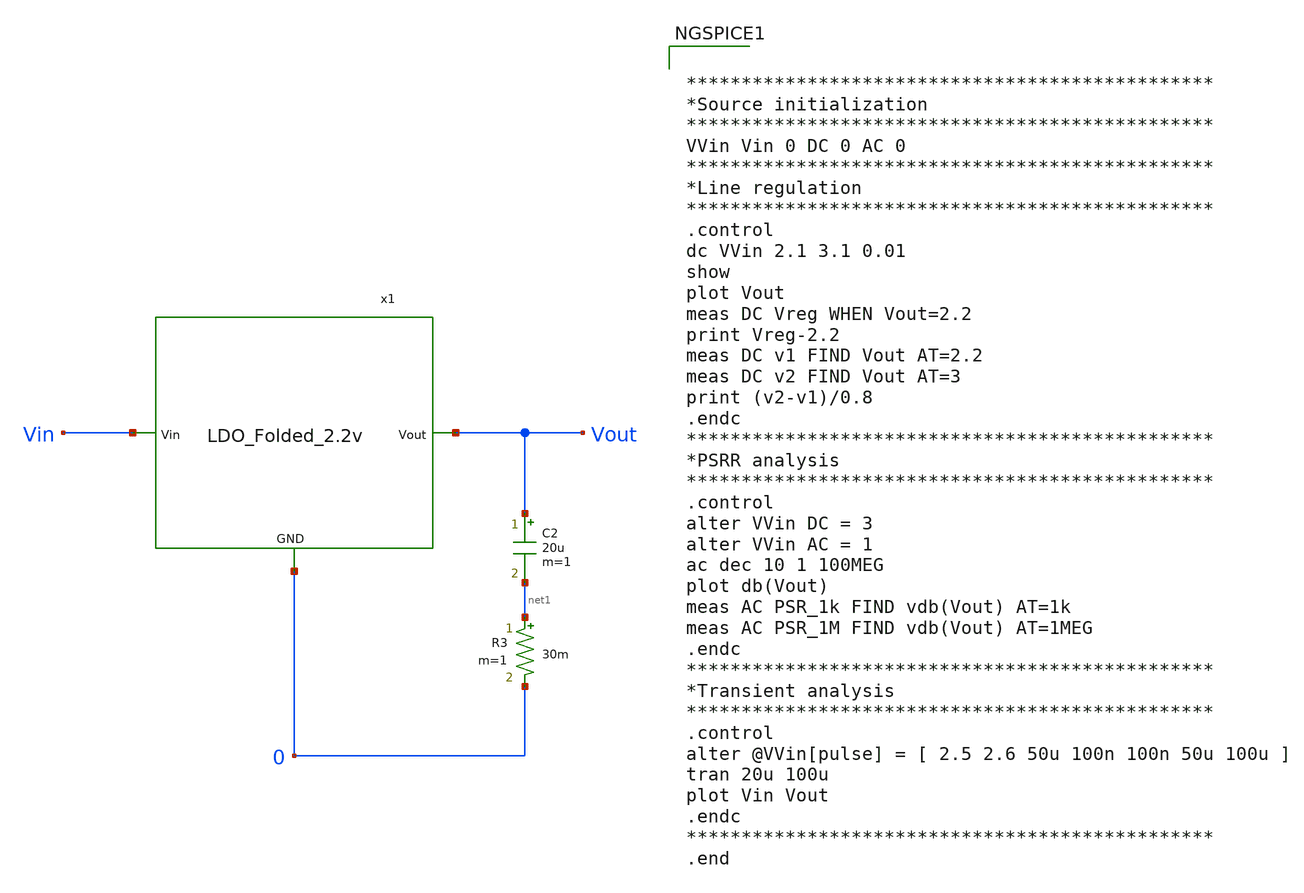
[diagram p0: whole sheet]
** sch_path: Analog_Blocks/LDO/Testbench/LDO_Folded_2.2v_meas.sch
**.subckt LDO_Folded_2.2v_meas
C2 Vout net1 20u m=1
R3 net1 0 30m m=1
x1 Vin Vout 0 LDO_Folded_2.2v
**** begin user architecture code


************************************************
*Source initialization
************************************************
VVin Vin 0 DC 0 AC 0
************************************************
*Line regulation
************************************************
.control
dc VVin 2.1 3.1 0.01
show
plot Vout
meas DC Vreg WHEN Vout=2.2
print Vreg-2.2
meas DC v1 FIND Vout AT=2.2
meas DC v2 FIND Vout AT=3
print (v2-v1)/0.8
.endc
************************************************
*PSRR analysis
************************************************
.control
alter VVin DC = 3
alter VVin AC = 1
ac dec 10 1 100MEG
plot db(Vout)
meas AC PSR_1k FIND vdb(Vout) AT=1k
meas AC PSR_1M FIND vdb(Vout) AT=1MEG
.endc
************************************************
*Transient analysis
************************************************
.control
alter @VVin[pulse] = [ 2.5 2.6 50u 100n 100n 50u 100u ]
tran 20u 100u
plot Vin Vout
.endc
************************************************
.end



.include ~/Analog_blocks/models/skywater-pdk/libraries/sky130_fd_pr/latest/cells/nfet_01v8/sky130_fd_pr__nfet_01v8__tt.corner.spice
.include ~/Analog_blocks/models/skywater-pdk/libraries/sky130_fd_pr/latest/cells/nfet_01v8_lvt/sky130_fd_pr__nfet_01v8_lvt__tt.corner.spice
.include ~/Analog_blocks/models/skywater-pdk/libraries/sky130_fd_pr/latest/cells/pfet_01v8/sky130_fd_pr__pfet_01v8__tt.corner.spice
.include ~/Analog_blocks/models/skywater-pdk/libraries/sky130_fd_pr/latest/cells/nfet_03v3_nvt/sky130_fd_pr__nfet_03v3_nvt__tt.corner.spice
.include ~/Analog_blocks/models/skywater-pdk/libraries/sky130_fd_pr/latest/cells/nfet_05v0_nvt/sky130_fd_pr__nfet_05v0_nvt__tt.corner.spice
.include ~/Analog_blocks/models/skywater-pdk/libraries/sky130_fd_pr/latest/cells/esd_nfet_01v8/sky130_fd_pr__esd_nfet_01v8__tt.corner.spice
.include ~/Analog_blocks/models/skywater-pdk/libraries/sky130_fd_pr/latest/cells/pfet_01v8_lvt/sky130_fd_pr__pfet_01v8_lvt__tt.corner.spice
.include ~/Analog_blocks/models/skywater-pdk/libraries/sky130_fd_pr/latest/cells/pfet_01v8_hvt/sky130_fd_pr__pfet_01v8_hvt__tt.corner.spice
.include ~/Analog_blocks/models/skywater-pdk/libraries/sky130_fd_pr/latest/cells/esd_pfet_g5v0d10v5/sky130_fd_pr__esd_pfet_g5v0d10v5__tt.corner.spice
.include ~/Analog_blocks/models/skywater-pdk/libraries/sky130_fd_pr/latest/cells/pfet_g5v0d10v5/sky130_fd_pr__pfet_g5v0d10v5__tt.corner.spice
.include ~/Analog_blocks/models/skywater-pdk/libraries/sky130_fd_pr/latest/cells/pfet_g5v0d16v0/sky130_fd_pr__pfet_g5v0d16v0__tt.corner.spice
.include ~/Analog_blocks/models/skywater-pdk/libraries/sky130_fd_pr/latest/cells/nfet_g5v0d10v5/sky130_fd_pr__nfet_g5v0d10v5__tt.corner.spice
.include ~/Analog_blocks/models/skywater-pdk/libraries/sky130_fd_pr/latest/cells/nfet_g5v0d16v0/sky130_fd_pr__nfet_g5v0d16v0__tt_discrete.corner.spice
.include ~/Analog_blocks/models/skywater-pdk/libraries/sky130_fd_pr/latest/cells/esd_nfet_g5v0d10v5/sky130_fd_pr__esd_nfet_g5v0d10v5__tt.corner.spice
.include ~/Analog_blocks/models/skywater-pdk/libraries/sky130_fd_pr/latest/models/corners/tt/nonfet.spice
* Mismatch parameters
.include ~/Analog_blocks/models/skywater-pdk/libraries/sky130_fd_pr/latest/cells/nfet_01v8/sky130_fd_pr__nfet_01v8__mismatch.corner.spice
.include ~/Analog_blocks/models/skywater-pdk/libraries/sky130_fd_pr/latest/cells/pfet_01v8/sky130_fd_pr__pfet_01v8__mismatch.corner.spice
.include ~/Analog_blocks/models/skywater-pdk/libraries/sky130_fd_pr/latest/cells/nfet_01v8_lvt/sky130_fd_pr__nfet_01v8_lvt__mismatch.corner.spice
.include ~/Analog_blocks/models/skywater-pdk/libraries/sky130_fd_pr/latest/cells/pfet_01v8_lvt/sky130_fd_pr__pfet_01v8_lvt__mismatch.corner.spice
.include ~/Analog_blocks/models/skywater-pdk/libraries/sky130_fd_pr/latest/cells/pfet_01v8_hvt/sky130_fd_pr__pfet_01v8_hvt__mismatch.corner.spice
.include ~/Analog_blocks/models/skywater-pdk/libraries/sky130_fd_pr/latest/cells/nfet_g5v0d10v5/sky130_fd_pr__nfet_g5v0d10v5__mismatch.corner.spice
.include ~/Analog_blocks/models/skywater-pdk/libraries/sky130_fd_pr/latest/cells/pfet_g5v0d10v5/sky130_fd_pr__pfet_g5v0d10v5__mismatch.corner.spice
.include ~/Analog_blocks/models/skywater-pdk/libraries/sky130_fd_pr/latest/cells/nfet_05v0_nvt/sky130_fd_pr__nfet_05v0_nvt__mismatch.corner.spice
.include ~/Analog_blocks/models/skywater-pdk/libraries/sky130_fd_pr/latest/cells/nfet_03v3_nvt/sky130_fd_pr__nfet_03v3_nvt__mismatch.corner.spice
* Resistor
.include ~/Analog_blocks/models/skywater-pdk/libraries/sky130_fd_pr/latest/models/r+c/res_typical__cap_typical.spice
.include ~/Analog_blocks/models/skywater-pdk/libraries/sky130_fd_pr/latest/models/r+c/res_typical__cap_typical__lin.spice
* Special cells
.include ~/Analog_blocks/models/skywater-pdk/libraries/sky130_fd_pr/latest/models/corners/tt/specialized_cells.spice
* All models
.include ~/Analog_blocks/models/skywater-pdk/libraries/sky130_fd_pr/latest/models/all.spice
* Corner
.include ~/Analog_blocks/models/skywater-pdk/libraries/sky130_fd_pr/latest/models/corners/tt/rf.spice

**** end user architecture code
**.ends

* expanding   symbol:
*+  /home/eslam/Analog_blocks/Analog_Blocks/LDO/Schematic/LDO_Folded_2.2v/LDO_Folded_2.2v.sym # of pins=3
** sym_path: Analog_blocks/Analog_Blocks/LDO/Schematic/LDO_Folded_2.2v/LDO_Folded_2.2v.sym
** sch_path: Analog_blocks/Analog_Blocks/LDO/Schematic/LDO_Folded_2.2v/LDO_Folded_2.2v.sch
.subckt LDO_Folded_2.2v Vin Vout GND
*.ipin Vin
*.ipin GND
*.opin Vout
XR1 net1 Vout GND sky130_fd_pr__res_xhigh_po W=1 L=60 mult=1 m=1
XR2 GND net1 GND sky130_fd_pr__res_xhigh_po W=1 L=50 mult=1 m=1
XC1 Vout net1 sky130_fd_pr__cap_mim_m3_2 W=1 L=1 MF=1 m=1
XM1 Vout net2 Vin Vin sky130_fd_pr__pfet_g5v0d10v5 L=0.5 W=20 nf=1 ad='int((nf+1)/2) * W/nf * 0.29' as='int((nf+2)/2) * W/nf * 0.29'
+ pd='2*int((nf+1)/2) * (W/nf + 0.29)' ps='2*int((nf+2)/2) * (W/nf + 0.29)' nrd='0.29 / W' nrs='0.29 / W'
+ sa=0 sb=0 sd=0 mult=1000 m=1000
x1 Vin net2 net1 net3 net3 GND Error_amplifier_Folded
x2 net3 Vin GND Bandgap5v
.ends


* expanding   symbol:
*+  /home/eslam/Analog_blocks/Analog_Blocks/LDO/Schematic/LDO_Folded_2.2v/Error_amplifier_Folded.sym # of pins=6
** sym_path: Analog_Blocks/LDO/Schematic/LDO_Folded_1.8v/Error_amplifier_Folded.sym
** sch_path: Analog_Blocks/LDO/Schematic/LDO_Folded_1.8v/Error_amplifier_Folded.sch
.subckt Error_amplifier_Folded VDD Vout Vp Vn Ibias GND
*.ipin VDD
*.ipin GND
*.ipin Vp
*.ipin Vn
*.opin Vout
*.ipin Ibias
XM1 net3 Vp net1 GND sky130_fd_pr__nfet_g5v0d10v5 L=0.5 W=50 nf=1 ad='int((nf+1)/2) * W/nf * 0.29' as='int((nf+2)/2) * W/nf * 0.29'
+ pd='2*int((nf+1)/2) * (W/nf + 0.29)' ps='2*int((nf+2)/2) * (W/nf + 0.29)' nrd='0.29 / W' nrs='0.29 / W'
+ sa=0 sb=0 sd=0 mult=1 m=1
XM2 net2 Vn net1 GND sky130_fd_pr__nfet_g5v0d10v5 L=0.5 W=50 nf=1 ad='int((nf+1)/2) * W/nf * 0.29' as='int((nf+2)/2) * W/nf * 0.29'
+ pd='2*int((nf+1)/2) * (W/nf + 0.29)' ps='2*int((nf+2)/2) * (W/nf + 0.29)' nrd='0.29 / W' nrs='0.29 / W'
+ sa=0 sb=0 sd=0 mult=1 m=1
XM9 Vout net4 GND GND sky130_fd_pr__nfet_g5v0d10v5 L=2 W=6 nf=1 ad='int((nf+1)/2) * W/nf * 0.29' as='int((nf+2)/2) * W/nf * 0.29'
+ pd='2*int((nf+1)/2) * (W/nf + 0.29)' ps='2*int((nf+2)/2) * (W/nf + 0.29)' nrd='0.29 / W' nrs='0.29 / W'
+ sa=0 sb=0 sd=0 mult=1 m=1
XM6 net4 net6 net3 VDD sky130_fd_pr__pfet_g5v0d10v5 L=0.5 W=40 nf=1 ad='int((nf+1)/2) * W/nf * 0.29'
+ as='int((nf+2)/2) * W/nf * 0.29' pd='2*int((nf+1)/2) * (W/nf + 0.29)' ps='2*int((nf+2)/2) * (W/nf + 0.29)'
+ nrd='0.29 / W' nrs='0.29 / W' sa=0 sb=0 sd=0 mult=1 m=1
XM5 net2 net5 VDD VDD sky130_fd_pr__pfet_g5v0d10v5 L=0.5 W=40 nf=1 ad='int((nf+1)/2) * W/nf * 0.29' as='int((nf+2)/2) * W/nf * 0.29'
+ pd='2*int((nf+1)/2) * (W/nf + 0.29)' ps='2*int((nf+2)/2) * (W/nf + 0.29)' nrd='0.29 / W' nrs='0.29 / W'
+ sa=0 sb=0 sd=0 mult=1 m=1
XM4 net3 net5 VDD VDD sky130_fd_pr__pfet_g5v0d10v5 L=0.5 W=40 nf=1 ad='int((nf+1)/2) * W/nf * 0.29' as='int((nf+2)/2) * W/nf * 0.29'
+ pd='2*int((nf+1)/2) * (W/nf + 0.29)' ps='2*int((nf+2)/2) * (W/nf + 0.29)' nrd='0.29 / W' nrs='0.29 / W'
+ sa=0 sb=0 sd=0 mult=1 m=1
XM3 net1 Ibias GND GND sky130_fd_pr__nfet_g5v0d10v5 L=0.9 W=12 nf=1 ad='int((nf+1)/2) * W/nf * 0.29'
+ as='int((nf+2)/2) * W/nf * 0.29' pd='2*int((nf+1)/2) * (W/nf + 0.29)' ps='2*int((nf+2)/2) * (W/nf + 0.29)'
+ nrd='0.29 / W' nrs='0.29 / W' sa=0 sb=0 sd=0 mult=1 m=1
XM7 Vout net6 net2 VDD sky130_fd_pr__pfet_g5v0d10v5 L=0.5 W=40 nf=1 ad='int((nf+1)/2) * W/nf * 0.29'
+ as='int((nf+2)/2) * W/nf * 0.29' pd='2*int((nf+1)/2) * (W/nf + 0.29)' ps='2*int((nf+2)/2) * (W/nf + 0.29)'
+ nrd='0.29 / W' nrs='0.29 / W' sa=0 sb=0 sd=0 mult=1 m=1
XM8 net4 net4 GND GND sky130_fd_pr__nfet_g5v0d10v5 L=2 W=6 nf=1 ad='int((nf+1)/2) * W/nf * 0.29' as='int((nf+2)/2) * W/nf * 0.29'
+ pd='2*int((nf+1)/2) * (W/nf + 0.29)' ps='2*int((nf+2)/2) * (W/nf + 0.29)' nrd='0.29 / W' nrs='0.29 / W'
+ sa=0 sb=0 sd=0 mult=1 m=1
XM10 Ibias Ibias GND GND sky130_fd_pr__nfet_g5v0d10v5 L=0.9 W=12 nf=1 ad='int((nf+1)/2) * W/nf * 0.29'
+ as='int((nf+2)/2) * W/nf * 0.29' pd='2*int((nf+1)/2) * (W/nf + 0.29)' ps='2*int((nf+2)/2) * (W/nf + 0.29)'
+ nrd='0.29 / W' nrs='0.29 / W' sa=0 sb=0 sd=0 mult=1 m=1
XM11 net5 Ibias GND GND sky130_fd_pr__nfet_g5v0d10v5 L=0.9 W=6 nf=1 ad='int((nf+1)/2) * W/nf * 0.29'
+ as='int((nf+2)/2) * W/nf * 0.29' pd='2*int((nf+1)/2) * (W/nf + 0.29)' ps='2*int((nf+2)/2) * (W/nf + 0.29)'
+ nrd='0.29 / W' nrs='0.29 / W' sa=0 sb=0 sd=0 mult=1 m=1
XM12 net6 Ibias GND GND sky130_fd_pr__nfet_g5v0d10v5 L=0.9 W=6 nf=1 ad='int((nf+1)/2) * W/nf * 0.29'
+ as='int((nf+2)/2) * W/nf * 0.29' pd='2*int((nf+1)/2) * (W/nf + 0.29)' ps='2*int((nf+2)/2) * (W/nf + 0.29)'
+ nrd='0.29 / W' nrs='0.29 / W' sa=0 sb=0 sd=0 mult=1 m=1
XM13 net5 net5 VDD VDD sky130_fd_pr__pfet_g5v0d10v5 L=0.5 W=13.5 nf=1 ad='int((nf+1)/2) * W/nf * 0.29'
+ as='int((nf+2)/2) * W/nf * 0.29' pd='2*int((nf+1)/2) * (W/nf + 0.29)' ps='2*int((nf+2)/2) * (W/nf + 0.29)'
+ nrd='0.29 / W' nrs='0.29 / W' sa=0 sb=0 sd=0 mult=1 m=1
XM14 net6 net6 VDD VDD sky130_fd_pr__pfet_g5v0d10v5 L=1 W=2 nf=1 ad='int((nf+1)/2) * W/nf * 0.29' as='int((nf+2)/2) * W/nf * 0.29'
+ pd='2*int((nf+1)/2) * (W/nf + 0.29)' ps='2*int((nf+2)/2) * (W/nf + 0.29)' nrd='0.29 / W' nrs='0.29 / W'
+ sa=0 sb=0 sd=0 mult=1 m=1
.ends


* expanding   symbol:
*+  /home/eslam/Analog_blocks/Analog_Blocks/LDO/Schematic/LDO_Folded_2.2v/Bandgap5v.sym # of pins=3
** sym_path: Analog_Blocks/Bandgap/Schematics/BGR5v/Bandgap5v.sym
** sch_path: Analog_Blocks/Bandgap/Schematics/BGR5v/Bandgap5v.sch
.subckt Bandgap5v Vref VDD GND
*.ipin VDD
*.ipin GND
*.opin Vref
XQ1 GND GND net3 sky130_fd_pr__pnp_05v5_W0p68L0p68 m=1
XQ2 GND GND net1 sky130_fd_pr__pnp_05v5_W0p68L0p68 m=1
XQ3 GND GND net1 sky130_fd_pr__pnp_05v5_W0p68L0p68 m=1
XQ4 GND GND net1 sky130_fd_pr__pnp_05v5_W0p68L0p68 m=1
XQ5 GND GND net1 sky130_fd_pr__pnp_05v5_W0p68L0p68 m=1
XQ6 GND GND net1 sky130_fd_pr__pnp_05v5_W0p68L0p68 m=1
XQ7 GND GND net1 sky130_fd_pr__pnp_05v5_W0p68L0p68 m=1
XQ8 GND GND net1 sky130_fd_pr__pnp_05v5_W0p68L0p68 m=1
XQ9 GND GND net1 sky130_fd_pr__pnp_05v5_W0p68L0p68 m=1
XM2 net4 net5 VDD VDD sky130_fd_pr__pfet_g5v0d10v5 L=1 W=10 nf=1 ad='int((nf+1)/2) * W/nf * 0.29' as='int((nf+2)/2) * W/nf * 0.29'
+ pd='2*int((nf+1)/2) * (W/nf + 0.29)' ps='2*int((nf+2)/2) * (W/nf + 0.29)' nrd='0.29 / W' nrs='0.29 / W'
+ sa=0 sb=0 sd=0 mult=1 m=1
XM3 net3 net4 VDD VDD sky130_fd_pr__pfet_g5v0d10v5 L=1 W=10 nf=1 ad='int((nf+1)/2) * W/nf * 0.29' as='int((nf+2)/2) * W/nf * 0.29'
+ pd='2*int((nf+1)/2) * (W/nf + 0.29)' ps='2*int((nf+2)/2) * (W/nf + 0.29)' nrd='0.29 / W' nrs='0.29 / W'
+ sa=0 sb=0 sd=0 mult=1 m=1
XM1 net4 net5 GND GND sky130_fd_pr__nfet_g5v0d10v5 L=40 W=1 nf=1 ad='int((nf+1)/2) * W/nf * 0.29' as='int((nf+2)/2) * W/nf * 0.29'
+ pd='2*int((nf+1)/2) * (W/nf + 0.29)' ps='2*int((nf+2)/2) * (W/nf + 0.29)' nrd='0.29 / W' nrs='0.29 / W'
+ sa=0 sb=0 sd=0 mult=1 m=1
XR1 net2 Vref GND sky130_fd_pr__res_high_po W=1 L=6 mult=1 m=1
XR3 net3 Vref GND sky130_fd_pr__res_high_po W=1 L=6 mult=1 m=1
XR2 net1 net2 GND sky130_fd_pr__res_high_po W=1 L=2.6 mult=1 m=1
x1 VDD net3 net2 Vref net5 GND Bandgap5v_OTA
.ends


* expanding   symbol:  /home/eslam/Analog_Design/LDO/Schematic/Bandgap5v_OTA.sym # of pins=6
** sym_path: LDO/Schematic/Bandgap5v_OTA.sym
** sch_path: LDO/Schematic/Bandgap5v_OTA.sch
.subckt Bandgap5v_OTA Vdd Vn Vp Ibias Vhigh Gnd
*.opin Ibias
*.ipin Vhigh
*.ipin Vdd
*.ipin Gnd
*.ipin Vn
*.ipin Vp
XM6 Ibias Vhigh Vdd Vdd sky130_fd_pr__pfet_g5v0d10v5 L=1 W=10 nf=1 ad='int((nf+1)/2) * W/nf * 0.29' as='int((nf+2)/2) * W/nf * 0.29'
+ pd='2*int((nf+1)/2) * (W/nf + 0.29)' ps='2*int((nf+2)/2) * (W/nf + 0.29)' nrd='0.29 / W' nrs='0.29 / W'
+ sa=0 sb=0 sd=0 mult=1 m=1
XM5 net3 Vhigh Vdd Vdd sky130_fd_pr__pfet_g5v0d10v5 L=1 W=10 nf=1 ad='int((nf+1)/2) * W/nf * 0.29' as='int((nf+2)/2) * W/nf * 0.29'
+ pd='2*int((nf+1)/2) * (W/nf + 0.29)' ps='2*int((nf+2)/2) * (W/nf + 0.29)' nrd='0.29 / W' nrs='0.29 / W'
+ sa=0 sb=0 sd=0 mult=1 m=1
XM7 Vhigh Vhigh Vdd Vdd sky130_fd_pr__pfet_g5v0d10v5 L=1 W=54 nf=1 ad='int((nf+1)/2) * W/nf * 0.29' as='int((nf+2)/2) * W/nf * 0.29'
+ pd='2*int((nf+1)/2) * (W/nf + 0.29)' ps='2*int((nf+2)/2) * (W/nf + 0.29)' nrd='0.29 / W' nrs='0.29 / W'
+ sa=0 sb=0 sd=0 mult=1 m=1
XM2 net1 Vp net3 Vdd sky130_fd_pr__pfet_g5v0d10v5 L=1 W=30 nf=1 ad='int((nf+1)/2) * W/nf * 0.29' as='int((nf+2)/2) * W/nf * 0.29'
+ pd='2*int((nf+1)/2) * (W/nf + 0.29)' ps='2*int((nf+2)/2) * (W/nf + 0.29)' nrd='0.29 / W' nrs='0.29 / W'
+ sa=0 sb=0 sd=0 mult=1 m=1
XM1 net2 Vn net3 Vdd sky130_fd_pr__pfet_g5v0d10v5 L=1 W=30 nf=1 ad='int((nf+1)/2) * W/nf * 0.29' as='int((nf+2)/2) * W/nf * 0.29'
+ pd='2*int((nf+1)/2) * (W/nf + 0.29)' ps='2*int((nf+2)/2) * (W/nf + 0.29)' nrd='0.29 / W' nrs='0.29 / W'
+ sa=0 sb=0 sd=0 mult=1 m=1
XM8 Vhigh net1 Gnd Gnd sky130_fd_pr__nfet_g5v0d10v5 L=0.5 W=75 nf=1 ad='int((nf+1)/2) * W/nf * 0.29'
+ as='int((nf+2)/2) * W/nf * 0.29' pd='2*int((nf+1)/2) * (W/nf + 0.29)' ps='2*int((nf+2)/2) * (W/nf + 0.29)'
+ nrd='0.29 / W' nrs='0.29 / W' sa=0 sb=0 sd=0 mult=1 m=1
XM4 net1 net2 Gnd Gnd sky130_fd_pr__nfet_g5v0d10v5 L=0.5 W=7.5 nf=1 ad='int((nf+1)/2) * W/nf * 0.29'
+ as='int((nf+2)/2) * W/nf * 0.29' pd='2*int((nf+1)/2) * (W/nf + 0.29)' ps='2*int((nf+2)/2) * (W/nf + 0.29)'
+ nrd='0.29 / W' nrs='0.29 / W' sa=0 sb=0 sd=0 mult=1 m=1
XM3 net2 net2 Gnd Gnd sky130_fd_pr__nfet_g5v0d10v5 L=0.5 W=7.5 nf=1 ad='int((nf+1)/2) * W/nf * 0.29'
+ as='int((nf+2)/2) * W/nf * 0.29' pd='2*int((nf+1)/2) * (W/nf + 0.29)' ps='2*int((nf+2)/2) * (W/nf + 0.29)'
+ nrd='0.29 / W' nrs='0.29 / W' sa=0 sb=0 sd=0 mult=1 m=1
XC1 net1 Vhigh sky130_fd_pr__cap_mim_m3_2 W=1 L=1 MF=1 m=1
.ends

.end
